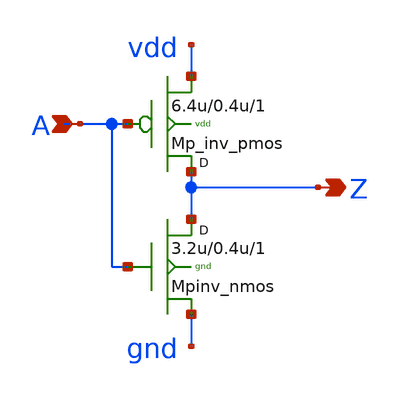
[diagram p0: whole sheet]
** sch_path: sram_4_16_scn4m/pinv_1.sch
**.subckt pinv_1 A Z
*.ipin A
*.opin Z
Mpinv_nmos Z A gnd gnd n w=3.2u l=0.4u m=1
Mp_inv_pmos Z A vdd vdd p w=6.4u l=0.4u m=1
**.ends
.end
